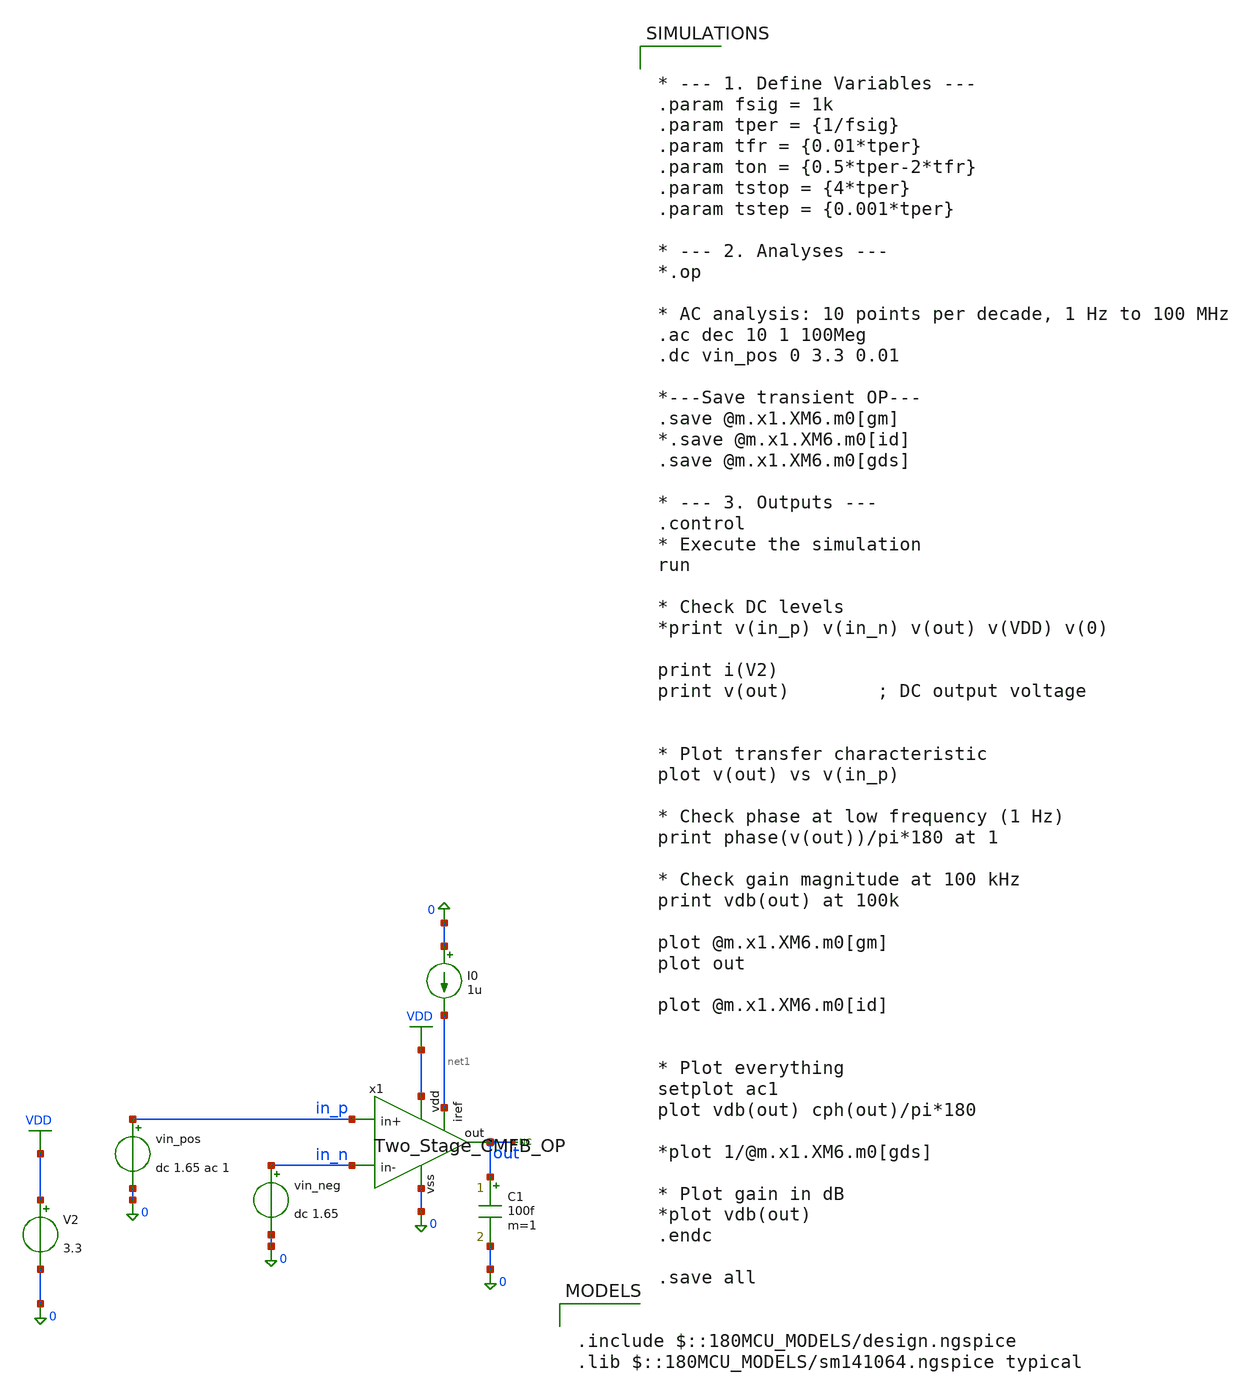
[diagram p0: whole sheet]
** sch_path: General/ADC/OTA/TB_OP_Amp.sch
**.subckt TB_OP_Amp
vin_pos in_p 0 dc 1.65 ac 1
V2 VDD 0 3.3
.save i(v2)
* noconn out
vin_neg in_n 0 dc 1.65
C1 out 0 100f m=1
I0 0 net1 1u
x1 out in_n in_p VDD 0 net1 Two_Stage_CMFB_OP
**** begin user architecture code

.include $::180MCU_MODELS/design.ngspice
.lib $::180MCU_MODELS/sm141064.ngspice typical



* --- 1. Define Variables ---
.param fsig = 1k
.param tper = {1/fsig}
.param tfr = {0.01*tper}
.param ton = {0.5*tper-2*tfr}
.param tstop = {4*tper}
.param tstep = {0.001*tper}

* --- 2. Analyses ---
*.op

* AC analysis: 10 points per decade, 1 Hz to 100 MHz
.ac dec 10 1 100Meg
.dc vin_pos 0 3.3 0.01

*---Save transient OP---
.save @m.x1.XM6.m0[gm]
*.save @m.x1.XM6.m0[id]
.save @m.x1.XM6.m0[gds]

* --- 3. Outputs ---
.control
* Execute the simulation
run

* Check DC levels
*print v(in_p) v(in_n) v(out) v(VDD) v(0)

print i(V2)
print v(out)        ; DC output voltage


* Plot transfer characteristic
plot v(out) vs v(in_p)

* Check phase at low frequency (1 Hz)
print phase(v(out))/pi*180 at 1

* Check gain magnitude at 100 kHz
print vdb(out) at 100k

plot @m.x1.XM6.m0[gm]
plot out

plot @m.x1.XM6.m0[id]


* Plot everything
setplot ac1
plot vdb(out) cph(out)/pi*180

*plot 1/@m.x1.XM6.m0[gds]

* Plot gain in dB
*plot vdb(out)
.endc

.save all


**** end user architecture code
**.ends

* expanding   symbol:  adc/OTA/Two_Stage_CMFB_OP.sym # of pins=6
** sym_path: Marcel/designs/Two_Stage_CMFB_OP.sym
** sch_path: Marcel/designs/Two_Stage_CMFB_OP.sch
.subckt Two_Stage_CMFB_OP out in- in+ vdd vss iref
*.opin out
*.ipin in-
*.ipin in+
*.iopin vdd
*.iopin vss
*.iopin iref
XM3 out in- net2 net2 pfet_03v3 L=2u W=5u nf=1 ad='int((nf+1)/2) * W/nf * 0.18u' as='int((nf+2)/2) * W/nf * 0.18u'
+ pd='2*int((nf+1)/2) * (W/nf + 0.18u)' ps='2*int((nf+2)/2) * (W/nf + 0.18u)' nrd='0.18u / W' nrs='0.18u / W'
+ sa=0 sb=0 sd=0 m=1
XM4 out in- net1 net1 pfet_03v3 L=2u W=5u nf=1 ad='int((nf+1)/2) * W/nf * 0.18u' as='int((nf+2)/2) * W/nf * 0.18u'
+ pd='2*int((nf+1)/2) * (W/nf + 0.18u)' ps='2*int((nf+2)/2) * (W/nf + 0.18u)' nrd='0.18u / W' nrs='0.18u / W'
+ sa=0 sb=0 sd=0 m=1
XM5 net3 in+ net1 net1 pfet_03v3 L=1u W=80u nf=1 ad='int((nf+1)/2) * W/nf * 0.18u' as='int((nf+2)/2) * W/nf * 0.18u'
+ pd='2*int((nf+1)/2) * (W/nf + 0.18u)' ps='2*int((nf+2)/2) * (W/nf + 0.18u)' nrd='0.18u / W' nrs='0.18u / W'
+ sa=0 sb=0 sd=0 m=1
XM6 net3 in+ net2 net2 pfet_03v3 L=1u W=80u nf=1 ad='int((nf+1)/2) * W/nf * 0.18u' as='int((nf+2)/2) * W/nf * 0.18u'
+ pd='2*int((nf+1)/2) * (W/nf + 0.18u)' ps='2*int((nf+2)/2) * (W/nf + 0.18u)' nrd='0.18u / W' nrs='0.18u / W'
+ sa=0 sb=0 sd=0 m=1
XM9 iref iref vss vss nfet_03v3 L=2u W=1u nf=1 ad='int((nf+1)/2) * W/nf * 0.18u' as='int((nf+2)/2) * W/nf * 0.18u'
+ pd='2*int((nf+1)/2) * (W/nf + 0.18u)' ps='2*int((nf+2)/2) * (W/nf + 0.18u)' nrd='0.18u / W' nrs='0.18u / W'
+ sa=0 sb=0 sd=0 m=1
XM10 out out vss vss nfet_03v3 L=2u W=10u nf=1 ad='int((nf+1)/2) * W/nf * 0.18u' as='int((nf+2)/2) * W/nf * 0.18u'
+ pd='2*int((nf+1)/2) * (W/nf + 0.18u)' ps='2*int((nf+2)/2) * (W/nf + 0.18u)' nrd='0.18u / W' nrs='0.18u / W'
+ sa=0 sb=0 sd=0 m=1
XM12 in- in- vdd vdd pfet_03v3 L=4u W=2u nf=1 ad='int((nf+1)/2) * W/nf * 0.18u' as='int((nf+2)/2) * W/nf * 0.18u'
+ pd='2*int((nf+1)/2) * (W/nf + 0.18u)' ps='2*int((nf+2)/2) * (W/nf + 0.18u)' nrd='0.18u / W' nrs='0.18u / W'
+ sa=0 sb=0 sd=0 m=1
XM14 in- iref vss vss nfet_03v3 L=2u W=1u nf=1 ad='int((nf+1)/2) * W/nf * 0.18u' as='int((nf+2)/2) * W/nf * 0.18u'
+ pd='2*int((nf+1)/2) * (W/nf + 0.18u)' ps='2*int((nf+2)/2) * (W/nf + 0.18u)' nrd='0.18u / W' nrs='0.18u / W'
+ sa=0 sb=0 sd=0 m=1
XM7 net3 net3 vss vss nfet_03v3 L=2u W=10u nf=1 ad='int((nf+1)/2) * W/nf * 0.18u' as='int((nf+2)/2) * W/nf * 0.18u'
+ pd='2*int((nf+1)/2) * (W/nf + 0.18u)' ps='2*int((nf+2)/2) * (W/nf + 0.18u)' nrd='0.18u / W' nrs='0.18u / W'
+ sa=0 sb=0 sd=0 m=1
XM8 net2 in- vdd vdd pfet_03v3 L=2u W=5u nf=1 ad='int((nf+1)/2) * W/nf * 0.18u' as='int((nf+2)/2) * W/nf * 0.18u'
+ pd='2*int((nf+1)/2) * (W/nf + 0.18u)' ps='2*int((nf+2)/2) * (W/nf + 0.18u)' nrd='0.18u / W' nrs='0.18u / W'
+ sa=0 sb=0 sd=0 m=1
XM11 net1 in- vdd vdd pfet_03v3 L=2u W=5u nf=1 ad='int((nf+1)/2) * W/nf * 0.18u' as='int((nf+2)/2) * W/nf * 0.18u'
+ pd='2*int((nf+1)/2) * (W/nf + 0.18u)' ps='2*int((nf+2)/2) * (W/nf + 0.18u)' nrd='0.18u / W' nrs='0.18u / W'
+ sa=0 sb=0 sd=0 m=1
.ends

.GLOBAL VDD
.end
